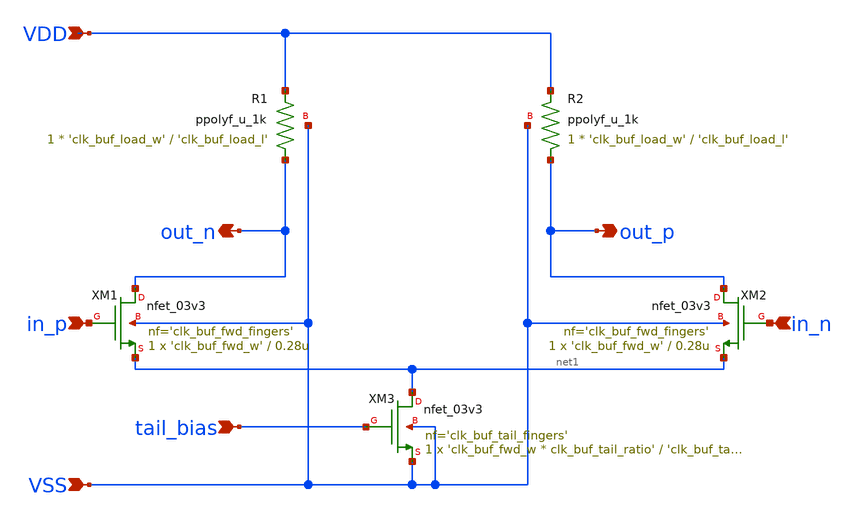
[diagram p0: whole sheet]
** sch_path: xschem/clk_buf.sch
**.subckt clk_buf VSS VDD out_n out_p in_p in_n tail_bias
*.ipin VSS
*.ipin VDD
*.opin out_n
*.opin out_p
*.ipin in_p
*.ipin in_n
*.ipin tail_bias
XM1 out_n in_p net1 VSS nfet_03v3 L=0.28u W='clk_buf_fwd_w' nf='clk_buf_fwd_fingers' ad='int((nf+1)/2) * W/nf * 0.18u'
+ as='int((nf+2)/2) * W/nf * 0.18u' pd='2*int((nf+1)/2) * (W/nf + 0.18u)' ps='2*int((nf+2)/2) * (W/nf + 0.18u)'
+ nrd='0.18u / W' nrs='0.18u / W' sa=0 sb=0 sd=0 m=1
XM3 net1 tail_bias VSS VSS nfet_03v3 L='clk_buf_tail_l' W='clk_buf_fwd_w * clk_buf_tail_ratio' nf='clk_buf_tail_fingers'
+ ad='int((nf+1)/2) * W/nf * 0.18u' as='int((nf+2)/2) * W/nf * 0.18u' pd='2*int((nf+1)/2) * (W/nf + 0.18u)'
+ ps='2*int((nf+2)/2) * (W/nf + 0.18u)' nrd='0.18u / W' nrs='0.18u / W' sa=0 sb=0 sd=0 m=1
XM2 out_p in_n net1 VSS nfet_03v3 L=0.28u W='clk_buf_fwd_w' nf='clk_buf_fwd_fingers' ad='int((nf+1)/2) * W/nf * 0.18u'
+ as='int((nf+2)/2) * W/nf * 0.18u' pd='2*int((nf+1)/2) * (W/nf + 0.18u)' ps='2*int((nf+2)/2) * (W/nf + 0.18u)'
+ nrd='0.18u / W' nrs='0.18u / W' sa=0 sb=0 sd=0 m=1
XR1 out_n VDD VSS ppolyf_u_1k r_width='clk_buf_load_w' r_length='clk_buf_load_l' m=1
XR2 out_p VDD VSS ppolyf_u_1k r_width='clk_buf_load_w' r_length='clk_buf_load_l' m=1
**.ends
.end
